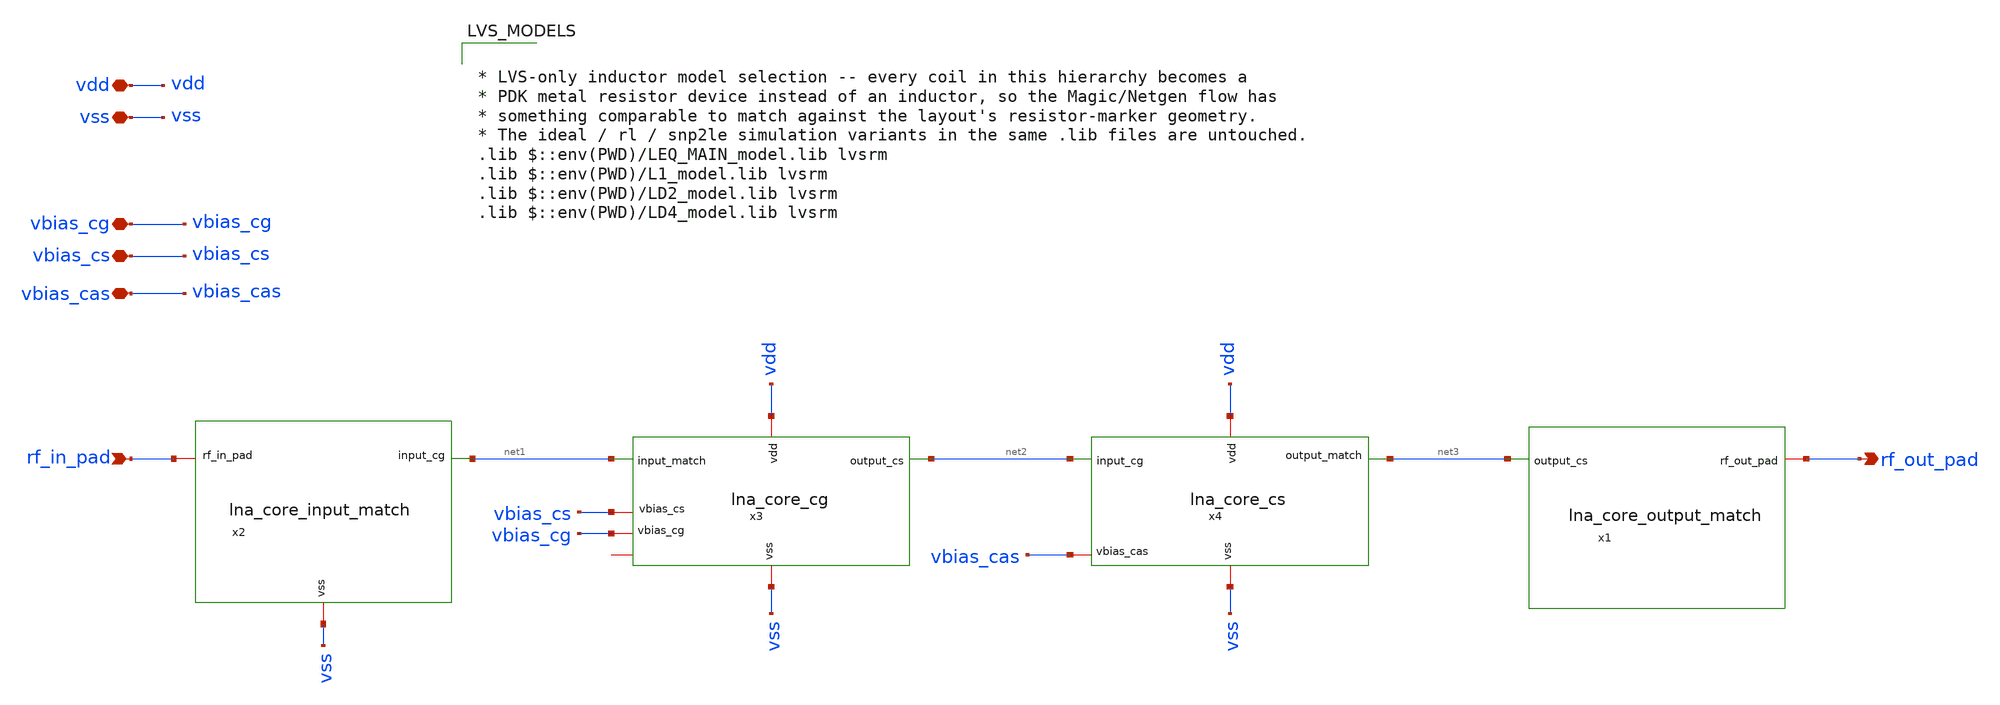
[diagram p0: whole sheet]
** sch_path: xschem/lna_core_parts.sch
**.subckt lna_core_parts rf_in_pad vbias_cg vbias_cs rf_out_pad vdd vss vbias_cas
*.ipin rf_in_pad
*.iopin vbias_cg
*.iopin vbias_cs
*.opin rf_out_pad
*.iopin vdd
*.iopin vss
*.iopin vbias_cas
x1 net3 rf_out_pad lna_core_output_match
x2 vss net1 rf_in_pad lna_core_input_match
x3 vbias_cs vdd vss vbias_cg net2 net1 lna_core_cg
x4 net3 vbias_cas net2 vdd vss lna_core_cs
**** begin user architecture code

* LVS-only inductor model selection -- every coil in this hierarchy becomes a
* PDK metal resistor device instead of an inductor, so the Magic/Netgen flow has
* something comparable to match against the layout's resistor-marker geometry.
* The ideal / rl / snp2le simulation variants in the same .lib files are untouched.
.lib $::env(PWD)/LEQ_MAIN_model.lib lvsrm
.lib $::env(PWD)/L1_model.lib lvsrm
.lib $::env(PWD)/LD2_model.lib lvsrm
.lib $::env(PWD)/LD4_model.lib lvsrm

**** end user architecture code
**.ends
.end
